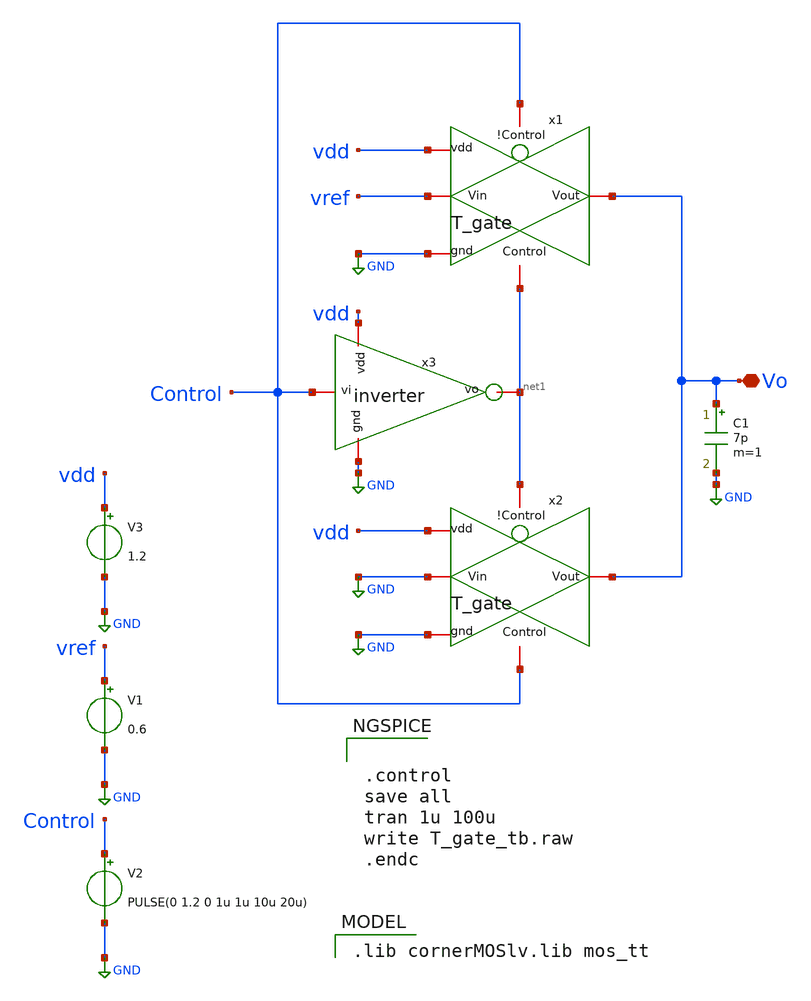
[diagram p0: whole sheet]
** sch_path: modules/module_3_8_bit_SAR_ADC/part_2_digital_comps/T_gate/testbench/T_gate_switch_tb.sch
**.subckt T_gate_switch_tb Vo
*.iopin Vo
V1 vref GND 0.6
V2 Control GND PULSE(0 1.2 0 1u 1u 10u 20u)
V3 vdd GND 1.2
x3 vdd Control net1 GND inverter
C1 Vo GND 7p m=1
x1 Control vref Vo GND net1 vdd T_gate
x2 net1 GND Vo GND Control vdd T_gate
**** begin user architecture code


.control
save all
tran 1u 100u
write T_gate_tb.raw
.endc


 .lib cornerMOSlv.lib mos_tt

**** end user architecture code
**.ends

* expanding   symbol:
*+  /home/pedersen/projects/IHP-AnalogAcademy/modules/module_3_8_bit_SAR_ADC/part_2_digital_comps/bootstrap_switch/schematic/inverter.sym # of pins=4
** sym_path: modules/module_3_8_bit_SAR_ADC/part_2_digital_comps/bootstrap_switch/schematic/inverter.sym
** sch_path: modules/module_3_8_bit_SAR_ADC/part_2_digital_comps/bootstrap_switch/schematic/inverter.sch
.subckt inverter vdd vi vo gnd
*.iopin vi
*.iopin vo
*.iopin gnd
*.iopin vdd
XM5 vo vi vdd vdd sg13_lv_pmos w=800n l=130n ng=1 m=1 mm_ok=1
XM7 vo vi gnd gnd sg13_lv_nmos w=400n l=130n ng=1 m=1 mm_ok=1
.ends


* expanding   symbol:
*+  /home/pedersen/projects/IHP-AnalogAcademy/modules/module_3_8_bit_SAR_ADC/part_2_digital_comps/T_gate/schematic/T_gate.sym # of pins=6
** sym_path: modules/module_3_8_bit_SAR_ADC/part_2_digital_comps/T_gate/schematic/T_gate.sym
** sch_path: modules/module_3_8_bit_SAR_ADC/part_2_digital_comps/T_gate/schematic/T_gate.sch
.subckt T_gate !Control Vin Vout gnd Control vdd
*.iopin Vout
*.iopin Vin
*.iopin !Control
*.iopin Control
*.iopin gnd
*.iopin vdd
XM1 Vin Control Vout gnd sg13_lv_nmos w=1u l=0.13u ng=1 m=1 mm_ok=1
XM2 Vin !Control Vout vdd sg13_lv_pmos w=2u l=0.13u ng=1 m=1 mm_ok=1
.ends

.GLOBAL GND
.end
